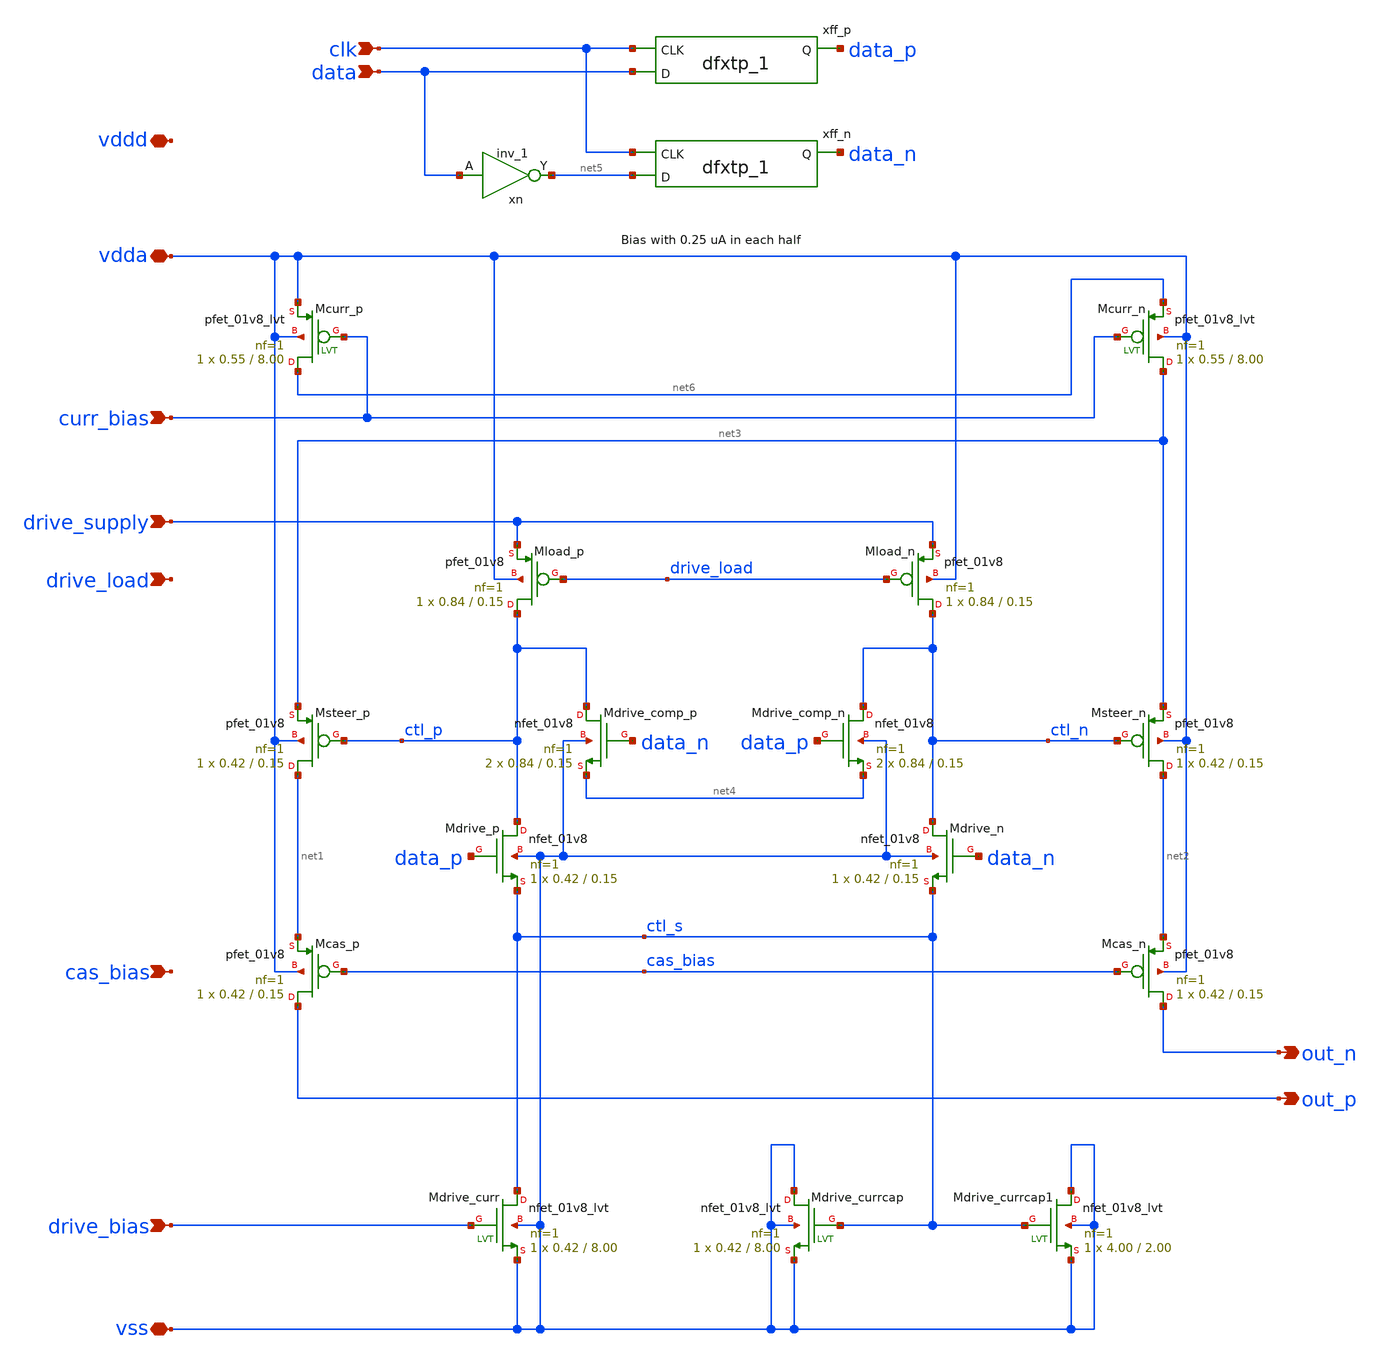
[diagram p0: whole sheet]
** sch_path: design/dac_unit_cell_quarter/dac_unit_cell_quarter.sch
**.subckt dac_unit_cell_quarter vdda vss curr_bias clk data drive_supply out_p out_n cas_bias
*+ drive_bias drive_load vddd
*.iopin vdda
*.iopin vss
*.ipin curr_bias
*.ipin clk
*.ipin data
*.ipin drive_supply
*.opin out_p
*.opin out_n
*.ipin cas_bias
*.ipin drive_bias
*.ipin drive_load
*.iopin vddd
XMcas_p out_p cas_bias net1 vdda sky130_fd_pr__pfet_01v8 L=0.15 W=0.42 nf=1 ad='W * 0.29' as='W * 0.29'
+ pd='2 * (W + 0.29)' ps='2 * (W + 0.29)' nrd='0.29 / W' nrs='0.29 / W' sa=0 sb=0 sd=0 mult=1 m=1
XMcas_n out_n cas_bias net2 vdda sky130_fd_pr__pfet_01v8 L=0.15 W=0.42 nf=1 ad='W * 0.29' as='W * 0.29'
+ pd='2 * (W + 0.29)' ps='2 * (W + 0.29)' nrd='0.29 / W' nrs='0.29 / W' sa=0 sb=0 sd=0 mult=1 m=1
XMcurr_p net6 curr_bias vdda vdda sky130_fd_pr__pfet_01v8_lvt L=8.00 W=0.55 nf=1 ad='int((nf+1)/2) * W/nf * 0.29'
+ as='int((nf+2)/2) * W/nf * 0.29' pd='2*int((nf+1)/2) * (W/nf + 0.29)' ps='2*int((nf+2)/2) * (W/nf + 0.29)'
+ nrd='0.29 / W' nrs='0.29 / W' sa=0 sb=0 sd=0 mult=1 m=1
XMcurr_n net3 curr_bias net6 vdda sky130_fd_pr__pfet_01v8_lvt L=8.00 W=0.55 nf=1 ad='int((nf+1)/2) * W/nf * 0.29'
+ as='int((nf+2)/2) * W/nf * 0.29' pd='2*int((nf+1)/2) * (W/nf + 0.29)' ps='2*int((nf+2)/2) * (W/nf + 0.29)'
+ nrd='0.29 / W' nrs='0.29 / W' sa=0 sb=0 sd=0 mult=1 m=1
XMsteer_p net1 ctl_p net3 vdda sky130_fd_pr__pfet_01v8 L=0.15 W=0.42 nf=1 ad='W * 0.29' as='W * 0.29'
+ pd='2 * (W + 0.29)' ps='2 * (W + 0.29)' nrd='0.29 / W' nrs='0.29 / W' sa=0 sb=0 sd=0 mult=1 m=1
XMsteer_n net2 ctl_n net3 vdda sky130_fd_pr__pfet_01v8 L=0.15 W=0.42 nf=1 ad='W * 0.29' as='W * 0.29'
+ pd='2 * (W + 0.29)' ps='2 * (W + 0.29)' nrd='0.29 / W' nrs='0.29 / W' sa=0 sb=0 sd=0 mult=1 m=1
XMdrive_p ctl_p data_p ctl_s vss sky130_fd_pr__nfet_01v8 L=0.15 W=0.42 nf=1 ad='int((nf+1)/2) * W/nf * 0.29'
+ as='int((nf+2)/2) * W/nf * 0.29' pd='2*int((nf+1)/2) * (W/nf + 0.29)' ps='2*int((nf+2)/2) * (W/nf + 0.29)'
+ nrd='0.29 / W' nrs='0.29 / W' sa=0 sb=0 sd=0 mult=1 m=1
XMdrive_n ctl_n data_n ctl_s vss sky130_fd_pr__nfet_01v8 L=0.15 W=0.42 nf=1 ad='int((nf+1)/2) * W/nf * 0.29'
+ as='int((nf+2)/2) * W/nf * 0.29' pd='2*int((nf+1)/2) * (W/nf + 0.29)' ps='2*int((nf+2)/2) * (W/nf + 0.29)'
+ nrd='0.29 / W' nrs='0.29 / W' sa=0 sb=0 sd=0 mult=1 m=1
XMdrive_comp_p ctl_p data_n net4 vss sky130_fd_pr__nfet_01v8 L=0.15 W=0.84 nf=1 ad='int((nf+1)/2) * W/nf * 0.29'
+ as='int((nf+2)/2) * W/nf * 0.29' pd='2*int((nf+1)/2) * (W/nf + 0.29)' ps='2*int((nf+2)/2) * (W/nf + 0.29)'
+ nrd='0.29 / W' nrs='0.29 / W' sa=0 sb=0 sd=0 mult=2 m=2
XMdrive_comp_n ctl_n data_p net4 vss sky130_fd_pr__nfet_01v8 L=0.15 W=0.84 nf=1 ad='int((nf+1)/2) * W/nf * 0.29'
+ as='int((nf+2)/2) * W/nf * 0.29' pd='2*int((nf+1)/2) * (W/nf + 0.29)' ps='2*int((nf+2)/2) * (W/nf + 0.29)'
+ nrd='0.29 / W' nrs='0.29 / W' sa=0 sb=0 sd=0 mult=2 m=2
xn data vss vss vddd vddd net5 sky130_fd_sc_hs__inv_1
xff_p clk data vss vss vddd vddd data_p sky130_fd_sc_hs__dfxtp_1
xff_n clk net5 vss vss vddd vddd data_n sky130_fd_sc_hs__dfxtp_1
XMload_p ctl_p drive_load drive_supply vdda sky130_fd_pr__pfet_01v8 L=0.15 W=0.84 nf=1 ad='W * 0.29'
+ as='W * 0.29' pd='2 * (W + 0.29)' ps='2 * (W + 0.29)' nrd='0.29 / W' nrs='0.29 / W' sa=0 sb=0 sd=0 mult=1
+ m=1
XMload_n ctl_n drive_load drive_supply vdda sky130_fd_pr__pfet_01v8 L=0.15 W=0.84 nf=1 ad='W * 0.29'
+ as='W * 0.29' pd='2 * (W + 0.29)' ps='2 * (W + 0.29)' nrd='0.29 / W' nrs='0.29 / W' sa=0 sb=0 sd=0 mult=1
+ m=1
XMdrive_curr ctl_s drive_bias vss vss sky130_fd_pr__nfet_01v8_lvt L=8.00 W=0.42 nf=1 ad='int((nf+1)/2) * W/nf * 0.29'
+ as='int((nf+2)/2) * W/nf * 0.29' pd='2*int((nf+1)/2) * (W/nf + 0.29)' ps='2*int((nf+2)/2) * (W/nf + 0.29)'
+ nrd='0.29 / W' nrs='0.29 / W' sa=0 sb=0 sd=0 mult=1 m=1
XMdrive_currcap vss ctl_s vss vss sky130_fd_pr__nfet_01v8_lvt L=8.00 W=0.42 nf=1 ad='int((nf+1)/2) * W/nf * 0.29'
+ as='int((nf+2)/2) * W/nf * 0.29' pd='2*int((nf+1)/2) * (W/nf + 0.29)' ps='2*int((nf+2)/2) * (W/nf + 0.29)'
+ nrd='0.29 / W' nrs='0.29 / W' sa=0 sb=0 sd=0 mult=1 m=1
XMdrive_currcap1 vss ctl_s vss vss sky130_fd_pr__nfet_01v8_lvt L=2.00 W=4.00 nf=1 ad='int((nf+1)/2) * W/nf * 0.29'
+ as='int((nf+2)/2) * W/nf * 0.29' pd='2*int((nf+1)/2) * (W/nf + 0.29)' ps='2*int((nf+2)/2) * (W/nf + 0.29)'
+ nrd='0.29 / W' nrs='0.29 / W' sa=0 sb=0 sd=0 mult=1 m=1
**.ends
.end
